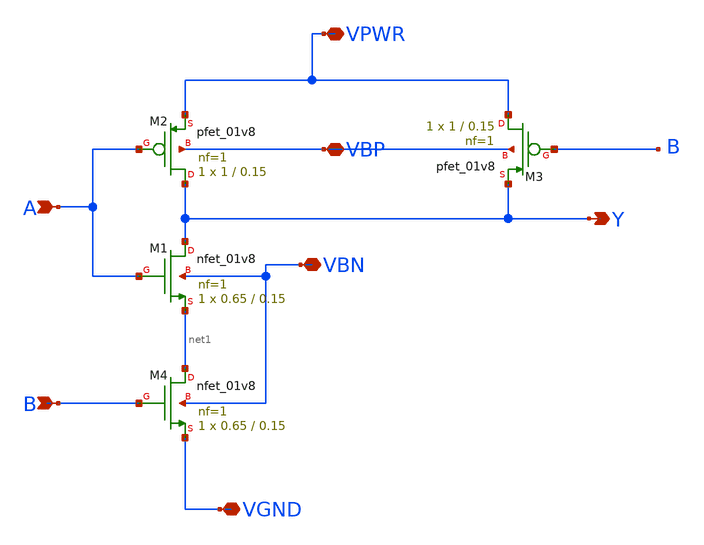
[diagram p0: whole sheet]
** sch_path: docs/_static/analog_flow_files/my_nand.sch
**.subckt my_nand VPWR VBP VBN VGND A B Y
*.iopin VPWR
*.iopin VBP
*.iopin VBN
*.iopin VGND
*.ipin A
*.ipin B
*.opin Y
XM1 Y A net1 VBN sky130_fd_pr__nfet_01v8 L=0.15 W=0.65 nf=1 ad='int((nf+1)/2) * W/nf * 0.29' as='int((nf+2)/2) * W/nf * 0.29'
+ pd='2*int((nf+1)/2) * (W/nf + 0.29)' ps='2*int((nf+2)/2) * (W/nf + 0.29)' nrd='0.29 / W' nrs='0.29 / W'
+ sa=0 sb=0 sd=0 mult=1 m=1
XM2 Y A VPWR VBP sky130_fd_pr__pfet_01v8 L=0.15 W=1 nf=1 ad='int((nf+1)/2) * W/nf * 0.29' as='int((nf+2)/2) * W/nf * 0.29'
+ pd='2*int((nf+1)/2) * (W/nf + 0.29)' ps='2*int((nf+2)/2) * (W/nf + 0.29)' nrd='0.29 / W' nrs='0.29 / W'
+ sa=0 sb=0 sd=0 mult=1 m=1
XM3 VPWR B Y VBP sky130_fd_pr__pfet_01v8 L=0.15 W=1 nf=1 ad='int((nf+1)/2) * W/nf * 0.29' as='int((nf+2)/2) * W/nf * 0.29'
+ pd='2*int((nf+1)/2) * (W/nf + 0.29)' ps='2*int((nf+2)/2) * (W/nf + 0.29)' nrd='0.29 / W' nrs='0.29 / W'
+ sa=0 sb=0 sd=0 mult=1 m=1
XM4 net1 B VGND VBN sky130_fd_pr__nfet_01v8 L=0.15 W=0.65 nf=1 ad='int((nf+1)/2) * W/nf * 0.29' as='int((nf+2)/2) * W/nf * 0.29'
+ pd='2*int((nf+1)/2) * (W/nf + 0.29)' ps='2*int((nf+2)/2) * (W/nf + 0.29)' nrd='0.29 / W' nrs='0.29 / W'
+ sa=0 sb=0 sd=0 mult=1 m=1
**.ends
.end
